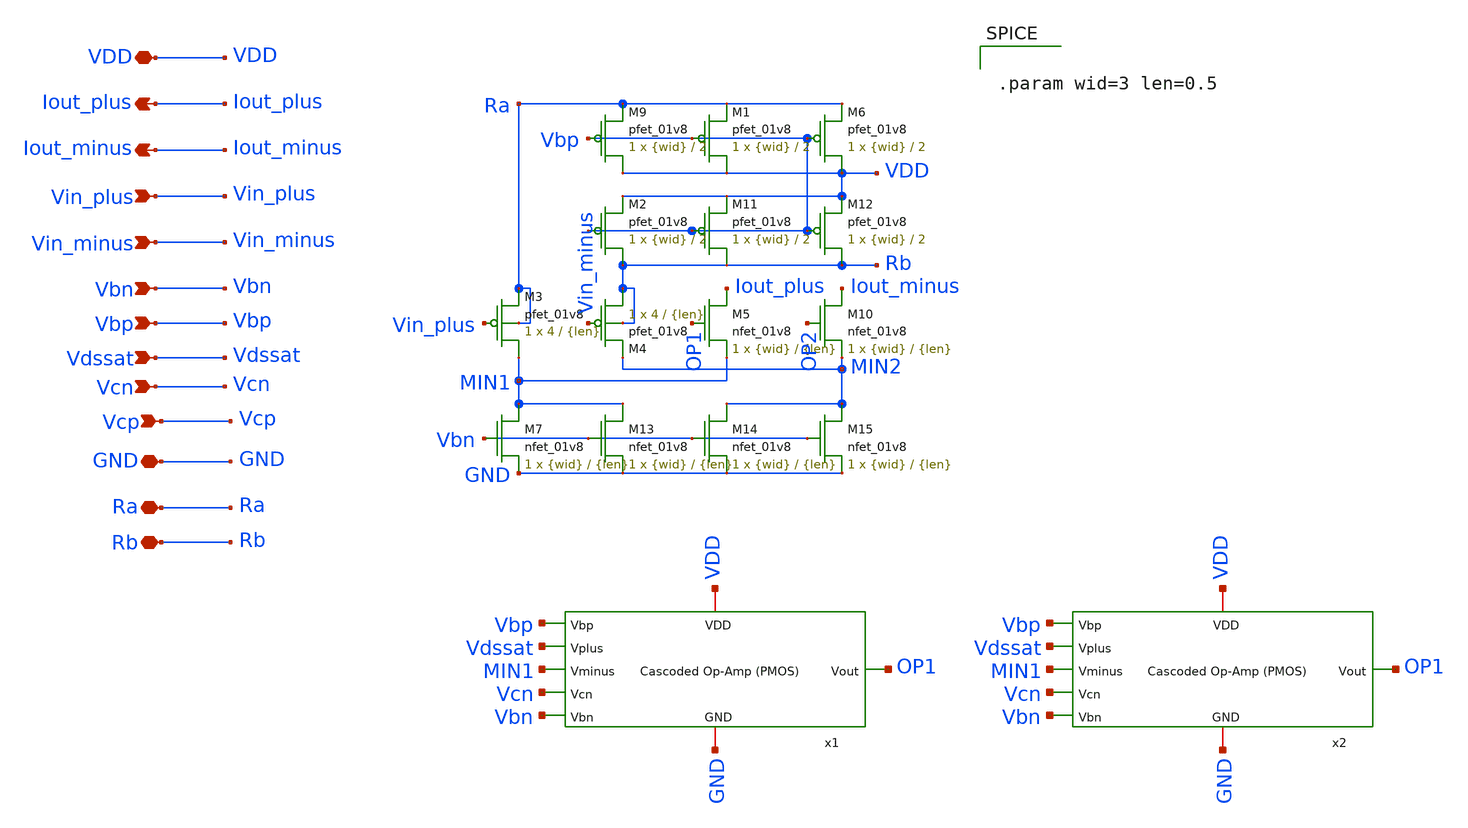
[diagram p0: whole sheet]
** sch_path: final/LDS/brad_VI_input_LDS.sch
**.subckt brad_VI_input_LDS Iout_plus Iout_minus VDD Vin_plus Vin_minus Vbn GND Ra Rb Vbp Vdssat Vcn
*+ Vcp
*.opin Iout_plus
*.opin Iout_minus
*.iopin VDD
*.ipin Vin_plus
*.ipin Vin_minus
*.ipin Vbn
*.iopin GND
*.iopin Ra
*.iopin Rb
*.ipin Vbp
*.ipin Vdssat
*.ipin Vcn
*.ipin Vcp
XM3 MIN1 Vin_plus Ra Ra sky130_fd_pr__pfet_01v8 L={len} W=4 nf=1 ad='int((nf+1)/2) * W/nf * 0.29' as='int((nf+2)/2) * W/nf * 0.29'
+ pd='2*int((nf+1)/2) * (W/nf + 0.29)' ps='2*int((nf+2)/2) * (W/nf + 0.29)' nrd='0.29 / W' nrs='0.29 / W'
+ sa=0 sb=0 sd=0 mult=1 m=1
XM5 Iout_plus OP1 MIN1 GND sky130_fd_pr__nfet_01v8 L={len} W={wid} nf=1 ad='int((nf+1)/2) * W/nf * 0.29'
+ as='int((nf+2)/2) * W/nf * 0.29' pd='2*int((nf+1)/2) * (W/nf + 0.29)' ps='2*int((nf+2)/2) * (W/nf + 0.29)'
+ nrd='0.29 / W' nrs='0.29 / W' sa=0 sb=0 sd=0 mult=1 m=1
XM4 Rb Vin_minus MIN2 Rb sky130_fd_pr__pfet_01v8 L={len} W=4 nf=1 ad='int((nf+1)/2) * W/nf * 0.29' as='int((nf+2)/2) * W/nf * 0.29'
+ pd='2*int((nf+1)/2) * (W/nf + 0.29)' ps='2*int((nf+2)/2) * (W/nf + 0.29)' nrd='0.29 / W' nrs='0.29 / W'
+ sa=0 sb=0 sd=0 mult=1 m=1
XM7 MIN1 Vbn GND GND sky130_fd_pr__nfet_01v8 L={len} W={wid} nf=1 ad='int((nf+1)/2) * W/nf * 0.29' as='int((nf+2)/2) * W/nf * 0.29'
+ pd='2*int((nf+1)/2) * (W/nf + 0.29)' ps='2*int((nf+2)/2) * (W/nf + 0.29)' nrd='0.29 / W' nrs='0.29 / W'
+ sa=0 sb=0 sd=0 mult=1 m=1
XM10 Iout_minus OP2 MIN2 GND sky130_fd_pr__nfet_01v8 L={len} W={wid} nf=1 ad='int((nf+1)/2) * W/nf * 0.29'
+ as='int((nf+2)/2) * W/nf * 0.29' pd='2*int((nf+1)/2) * (W/nf + 0.29)' ps='2*int((nf+2)/2) * (W/nf + 0.29)'
+ nrd='0.29 / W' nrs='0.29 / W' sa=0 sb=0 sd=0 mult=1 m=1
XM1 VDD Vbp Ra VDD sky130_fd_pr__pfet_01v8 L=2 W={wid} nf=1 ad='int((nf+1)/2) * W/nf * 0.29' as='int((nf+2)/2) * W/nf * 0.29'
+ pd='2*int((nf+1)/2) * (W/nf + 0.29)' ps='2*int((nf+2)/2) * (W/nf + 0.29)' nrd='0.29 / W' nrs='0.29 / W'
+ sa=0 sb=0 sd=0 mult=1 m=1
XM2 Rb Vbp VDD VDD sky130_fd_pr__pfet_01v8 L=2 W={wid} nf=1 ad='int((nf+1)/2) * W/nf * 0.29' as='int((nf+2)/2) * W/nf * 0.29'
+ pd='2*int((nf+1)/2) * (W/nf + 0.29)' ps='2*int((nf+2)/2) * (W/nf + 0.29)' nrd='0.29 / W' nrs='0.29 / W'
+ sa=0 sb=0 sd=0 mult=1 m=1
XM6 VDD Vbp Ra VDD sky130_fd_pr__pfet_01v8 L=2 W={wid} nf=1 ad='int((nf+1)/2) * W/nf * 0.29' as='int((nf+2)/2) * W/nf * 0.29'
+ pd='2*int((nf+1)/2) * (W/nf + 0.29)' ps='2*int((nf+2)/2) * (W/nf + 0.29)' nrd='0.29 / W' nrs='0.29 / W'
+ sa=0 sb=0 sd=0 mult=1 m=1
XM9 VDD Vbp Ra VDD sky130_fd_pr__pfet_01v8 L=2 W={wid} nf=1 ad='int((nf+1)/2) * W/nf * 0.29' as='int((nf+2)/2) * W/nf * 0.29'
+ pd='2*int((nf+1)/2) * (W/nf + 0.29)' ps='2*int((nf+2)/2) * (W/nf + 0.29)' nrd='0.29 / W' nrs='0.29 / W'
+ sa=0 sb=0 sd=0 mult=1 m=1
XM11 Rb Vbp VDD VDD sky130_fd_pr__pfet_01v8 L=2 W={wid} nf=1 ad='int((nf+1)/2) * W/nf * 0.29' as='int((nf+2)/2) * W/nf * 0.29'
+ pd='2*int((nf+1)/2) * (W/nf + 0.29)' ps='2*int((nf+2)/2) * (W/nf + 0.29)' nrd='0.29 / W' nrs='0.29 / W'
+ sa=0 sb=0 sd=0 mult=1 m=1
XM12 Rb Vbp VDD VDD sky130_fd_pr__pfet_01v8 L=2 W={wid} nf=1 ad='int((nf+1)/2) * W/nf * 0.29' as='int((nf+2)/2) * W/nf * 0.29'
+ pd='2*int((nf+1)/2) * (W/nf + 0.29)' ps='2*int((nf+2)/2) * (W/nf + 0.29)' nrd='0.29 / W' nrs='0.29 / W'
+ sa=0 sb=0 sd=0 mult=1 m=1
XM13 MIN1 Vbn GND GND sky130_fd_pr__nfet_01v8 L={len} W={wid} nf=1 ad='int((nf+1)/2) * W/nf * 0.29' as='int((nf+2)/2) * W/nf * 0.29'
+ pd='2*int((nf+1)/2) * (W/nf + 0.29)' ps='2*int((nf+2)/2) * (W/nf + 0.29)' nrd='0.29 / W' nrs='0.29 / W'
+ sa=0 sb=0 sd=0 mult=1 m=1
XM14 MIN2 Vbn GND GND sky130_fd_pr__nfet_01v8 L={len} W={wid} nf=1 ad='int((nf+1)/2) * W/nf * 0.29' as='int((nf+2)/2) * W/nf * 0.29'
+ pd='2*int((nf+1)/2) * (W/nf + 0.29)' ps='2*int((nf+2)/2) * (W/nf + 0.29)' nrd='0.29 / W' nrs='0.29 / W'
+ sa=0 sb=0 sd=0 mult=1 m=1
XM15 MIN2 Vbn GND GND sky130_fd_pr__nfet_01v8 L={len} W={wid} nf=1 ad='int((nf+1)/2) * W/nf * 0.29' as='int((nf+2)/2) * W/nf * 0.29'
+ pd='2*int((nf+1)/2) * (W/nf + 0.29)' ps='2*int((nf+2)/2) * (W/nf + 0.29)' nrd='0.29 / W' nrs='0.29 / W'
+ sa=0 sb=0 sd=0 mult=1 m=1
x1 Vbp Vdssat MIN1 Vcn Vbn VDD GND OP1 cascoded_opamp_pmos_LDS
x2 Vbp Vdssat MIN1 Vcn Vbn VDD GND OP1 cascoded_opamp_pmos_LDS
**** begin user architecture code


.param wid=3 len=0.5


**** end user architecture code
**.ends
.end
